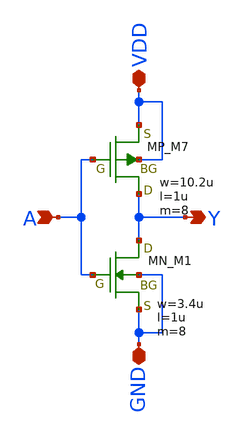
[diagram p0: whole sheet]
** sch_path: libs.tech/xschem/TR-1um_5_stdcell/INV_X8.sch
**.subckt INV_X8 A Y GND VDD
*.ipin A
*.opin Y
*.iopin GND
*.iopin VDD
XM7 Y A VDD VDD PMOS w=10.2u l=1u nrd=0 nrs=0 m=8
XM1 Y A GND GND NMOS w=3.4u l=1u nrd=0 nrs=0 m=8
**.ends
.end
